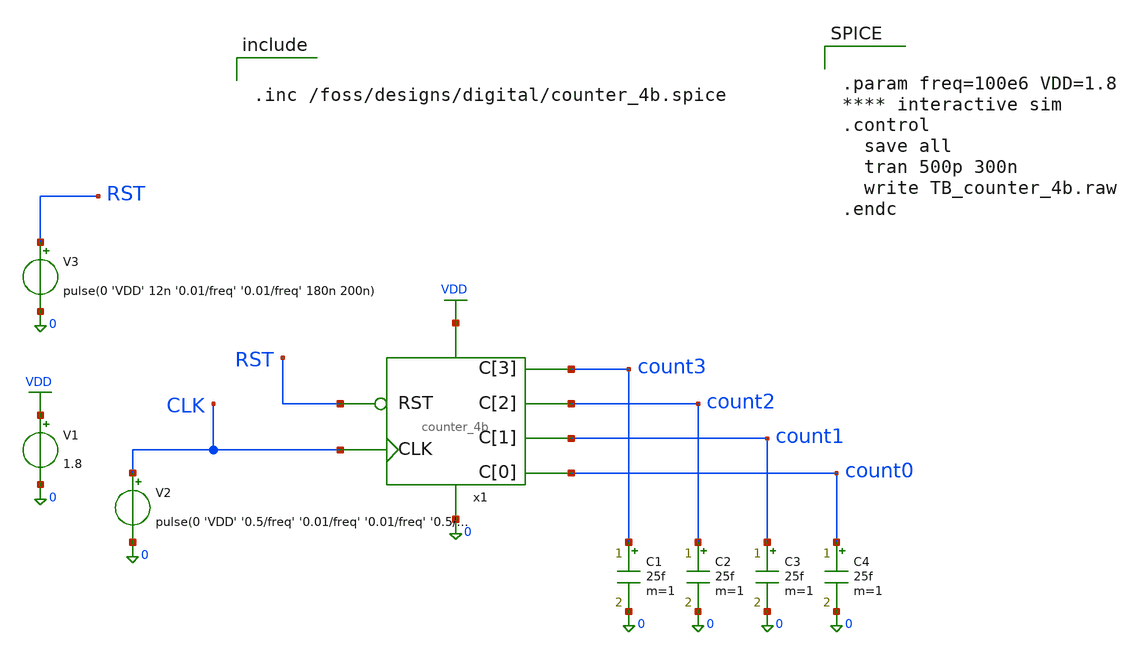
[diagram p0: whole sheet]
** sch_path: sky130A/analog/TB_counter_4b.sch
.lib $::SKYWATER_MODELS/sky130.lib.spice tt
.include $::SKYWATER_STDCELLS/sky130_fd_sc_hd.spice

**.subckt TB_counter_4b
V1 VDD 0 1.8
V2 CLK 0 pulse(0 'VDD' '0.5/freq' '0.01/freq' '0.01/freq' '0.5/freq' '1/freq')
C1 count3 0 25f m=1
C2 count2 0 25f m=1
C3 count1 0 25f m=1
C4 count0 0 25f m=1
V3 RST 0 pulse(0 'VDD' 12n '0.01/freq' '0.01/freq' 180n 200n)
x1 0 VDD CLK count0 count1 count2 count3 RST counter_4b
**** begin user architecture code


.inc /foss/designs/digital/counter_4b.spice




.param freq=100e6 VDD=1.8
**** interactive sim
.control
  save all
  tran 500p 300n
  write TB_counter_4b.raw
.endc


**** end user architecture code
**.ends
.GLOBAL VDD
.end
